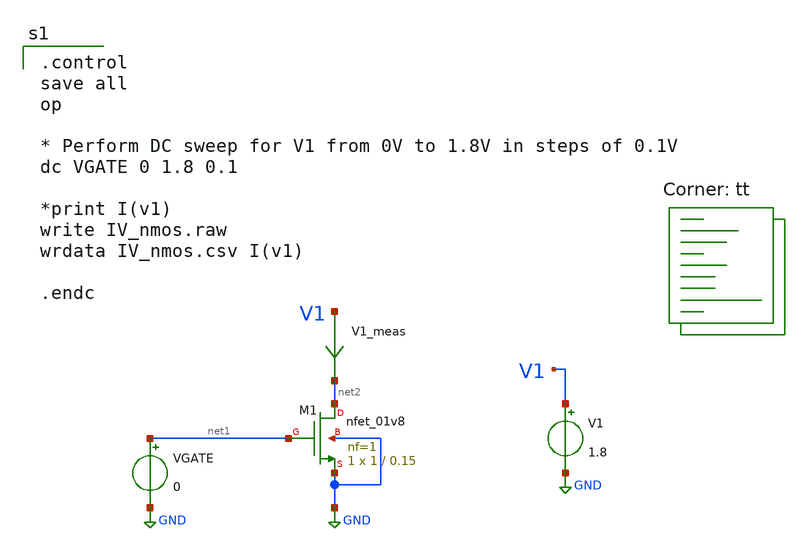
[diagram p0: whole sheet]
** sch_path: circuits/nch/IV_current_vs_vdrain/IV_current_vs_vdrain.sch
**.subckt IV_current_vs_vdrain
VGATE net1 GND 0
XM1 net2 net1 GND GND sky130_fd_pr__nfet_01v8 L=0.15 W=1 nf=1 ad='int((nf+1)/2) * W/nf * 0.29' as='int((nf+2)/2) * W/nf * 0.29'
+ pd='2*int((nf+1)/2) * (W/nf + 0.29)' ps='2*int((nf+2)/2) * (W/nf + 0.29)' nrd='0.29 / W' nrs='0.29 / W'
+ sa=0 sb=0 sd=0 mult=1 m=1
V1 V1 GND 1.8
V1_meas V1 net2 0
.save i(v1_meas)
**** begin user architecture code

.control
save all
op

* Perform DC sweep for V1 from 0V to 1.8V in steps of 0.1V
dc VGATE 0 1.8 0.1

*print I(v1)
write IV_nmos.raw
wrdata IV_nmos.csv I(v1)

.endc


.lib $::SKYWATER_MODELS/sky130.lib.spice tt
**** end user architecture code
**.ends
.GLOBAL GND
.end
